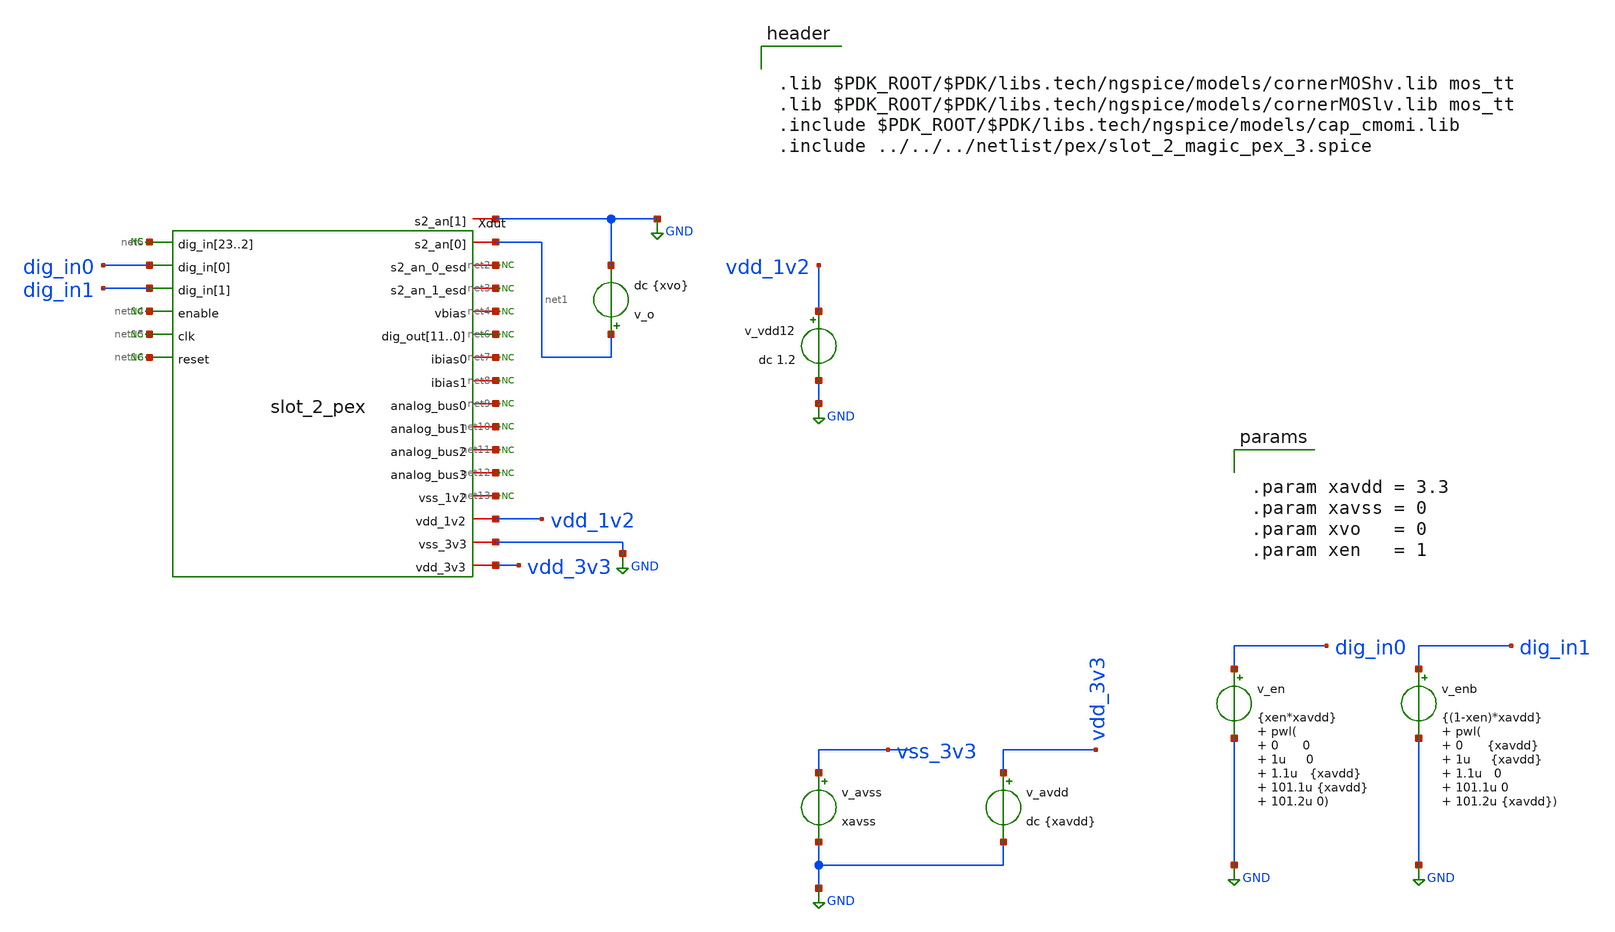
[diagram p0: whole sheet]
** sch_path: testbenches/xschem/tb_slot_2_tran.sch
**.subckt tb_slot_2_tran
Xdut net1 GND net2 net3 net4 net5 net5 net5 net5 net5 net5 net5 net5 net5 net5 net5 net5 net5 net5
+ net5 net5 net5 net5 net5 net5 net5 net5 dig_in0 net6 net6 net6 net6 net6 net6 net6 net6 net6 net6 net6
+ net6 dig_in1 net7 net8 net9 net10 net11 net12 net13 vdd_1v2 GND vdd_3v3 net14 net15 net16 slot_2_pex
v_avss vss_3v3 GND xavss
v_avdd vdd_3v3 GND dc {xavdd}
v_en dig_in0 GND {xen*xavdd} pwl( 0 0 1u 0 1.1u {xavdd} 101.1u {xavdd} 101.2u 0)
v_enb dig_in1 GND {(1-xen)*xavdd} pwl( 0 {xavdd} 1u {xavdd} 1.1u 0 101.1u 0 101.2u {xavdd})

v_o net1 GND dc {xvo}
v_vdd12 vdd_1v2 GND dc 1.2
* noconn #net13
* noconn #net12
* noconn #net11
* noconn #net10
* noconn #net9
* noconn #net8
* noconn #net7
* noconn #net6
* noconn #net4
* noconn #net3
* noconn #net2
* noconn #net5
* noconn #net16
* noconn #net15
* noconn #net14
**** begin user architecture code


.lib $PDK_ROOT/$PDK/libs.tech/ngspice/models/cornerMOShv.lib mos_tt
.lib $PDK_ROOT/$PDK/libs.tech/ngspice/models/cornerMOSlv.lib mos_tt
.include $PDK_ROOT/$PDK/libs.tech/ngspice/models/cap_cmomi.lib
.include ../../../netlist/pex/slot_2_magic_pex_3.spice




.option cshunt = 1e-15
.option gmin   = 1e-10
.control
  pre_osdi .lib $PDK_ROOT/$PDK/libs.tech/ngspice/models/osdi/psp103_nqs.osdi

  tran 10n 102u 10n uic
  let io = i(v_o)
  plot io ylimit 0 5u
  plot dig_in0

  meas tran io_before_disable find io at=101.09u

  set wr_vecnames
  set wr_singlescale
  wrdata ../plot_simulations/data/@schname\.txt io
.endc




.param xavdd = 3.3
.param xavss = 0
.param xvo   = 0
.param xen   = 1


**** end user architecture code
**.ends
.GLOBAL GND
.end
